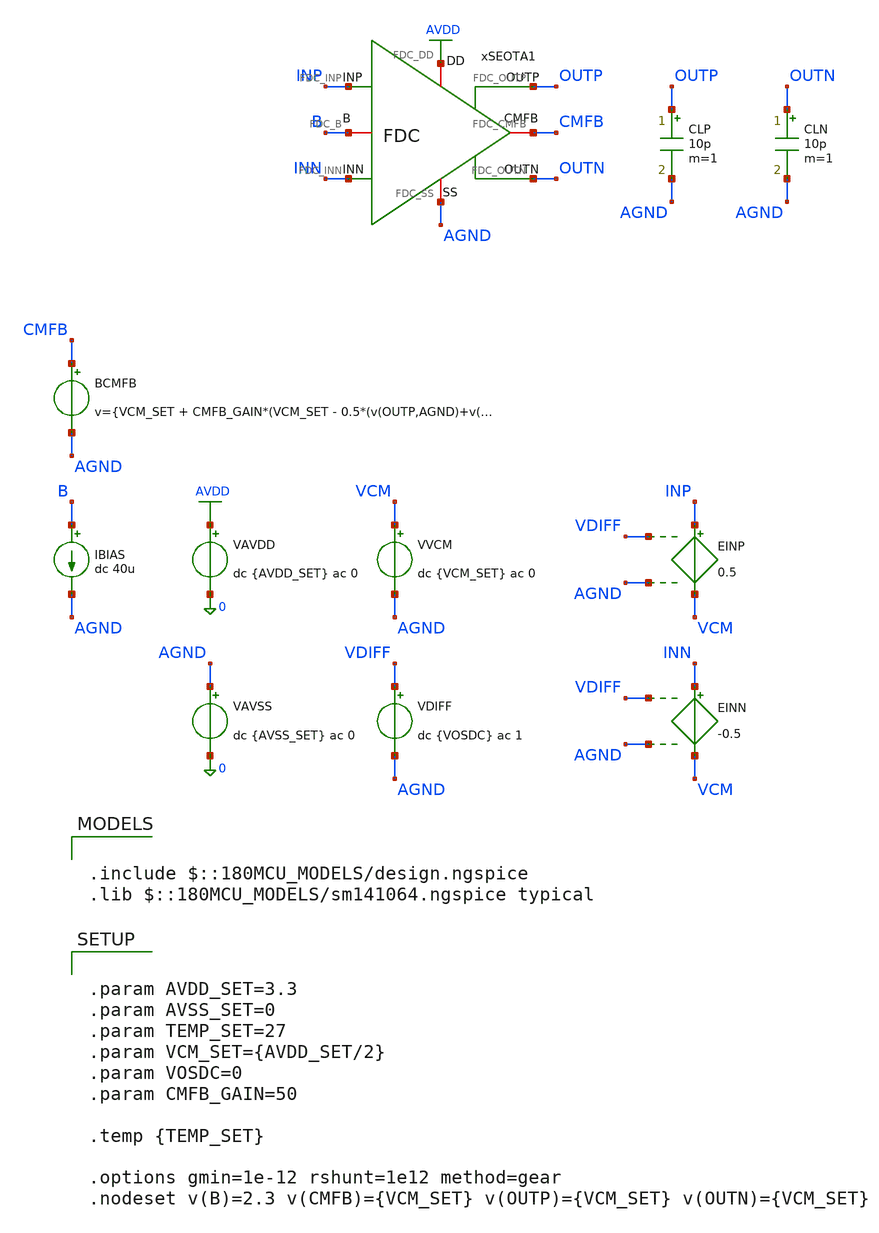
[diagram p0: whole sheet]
** sch_path: Design_Files/IC Design/Testbench/FD_OTA/FDC/Open_Loop/FDC_TB_OL_NOM.sch
**.subckt FDC_TB_OL_NOM
IBIAS B AGND dc 40u
VAVDD AVDD 0 dc {AVDD_SET} ac 0
.save i(vavdd)
CLP OUTP AGND 10p m=1
VVCM VCM AGND dc {VCM_SET} ac 0
VDIFF VDIFF AGND dc {VOSDC} ac 1
VAVSS AGND 0 dc {AVSS_SET} ac 0
.save i(vavss)
EINN INN VCM VDIFF AGND -0.5
EINP INP VCM VDIFF AGND 0.5
xSEOTA1 AVDD AGND INP INN OUTN B OUTP CMFB FDC
CLN OUTN AGND 10p m=1
BCMFB CMFB AGND v={VCM_SET + CMFB_GAIN*(VCM_SET - 0.5*(v(OUTP,AGND)+v(OUTN,AGND)))}
**** begin user architecture code

.include $::180MCU_MODELS/design.ngspice
.lib $::180MCU_MODELS/sm141064.ngspice typical



.control
destroy all
save all
set wr_vecnames
set wr_singlescale

shell mkdir -p
+ /foss/designs/ECG_Acquisition_IC/Measurement_Results/IC_Simulation/FD_OTA/FDC/NOM.Result_txt

shell rm -f
+ /foss/designs/ECG_Acquisition_IC/Measurement_Results/IC_Simulation/FD_OTA/FDC/NOM.Result_txt/NOM.ol_op.txt
shell rm -f
+ /foss/designs/ECG_Acquisition_IC/Measurement_Results/IC_Simulation/FD_OTA/FDC/NOM.Result_txt/NOM.ol_diff_tf.txt
shell rm -f
+ /foss/designs/ECG_Acquisition_IC/Measurement_Results/IC_Simulation/FD_OTA/FDC/NOM.Result_txt/NOM.ol_diff_ac.txt
shell rm -f
+ /foss/designs/ECG_Acquisition_IC/Measurement_Results/IC_Simulation/FD_OTA/FDC/NOM.Result_txt/NOM.ol_offset.txt
shell rm -f
+ /foss/designs/ECG_Acquisition_IC/Measurement_Results/IC_Simulation/FD_OTA/FDC/NOM.Result_txt/NOM.ol_icmr.txt
shell rm -f
+ /foss/designs/ECG_Acquisition_IC/Measurement_Results/IC_Simulation/FD_OTA/FDC/NOM.Result_txt/NOM.ol_cm_diff_ac.txt
shell rm -f
+ /foss/designs/ECG_Acquisition_IC/Measurement_Results/IC_Simulation/FD_OTA/FDC/NOM.Result_txt/NOM.ol_psrrp_diff_ac.txt
shell rm -f
+ /foss/designs/ECG_Acquisition_IC/Measurement_Results/IC_Simulation/FD_OTA/FDC/NOM.Result_txt/NOM.ol_psrrn_diff_ac.txt

let avdd_run = 3.3
let vcm_run  = avdd_run/2
let vos_run  = 0

* OP
alter @VVCM[DC] = $&vcm_run
alter @VDIFF[DC] = $&vos_run
alter @VVCM[ACMAG] = 0
alter @VDIFF[ACMAG] = 0
alter @VAVDD[ACMAG] = 0
alter @VAVSS[ACMAG] = 0

op

let op_vdd   = v(avdd) - v(agnd)
let op_vinp  = v(inp) - v(agnd)
let op_vinn  = v(inn) - v(agnd)
let op_voutp = v(outp) - v(agnd)
let op_voutn = v(outn) - v(agnd)
let op_ibias = 40e-6
let op_idd   = -vavdd#branch
let op_cmfb  = v(cmfb) - v(agnd)

wrdata
+ /foss/designs/ECG_Acquisition_IC/Measurement_Results/IC_Simulation/FD_OTA/FDC/NOM.Result_txt/NOM.ol_op.txt op_vdd op_vinp op_vinn op_voutp op_voutn op_ibias op_idd op_cmfb

* DC TF by low-frequency AC point
alter @VVCM[ACMAG] = 0
alter @VDIFF[ACMAG] = 1
alter @VDIFF[ACPHASE] = 0
alter @VAVDD[ACMAG] = 0
alter @VAVSS[ACMAG] = 0

ac lin 1 1 1

let tf_vod = v(outp) - v(outn)
let ad_dc = mag(tf_vod)

wrdata
+ /foss/designs/ECG_Acquisition_IC/Measurement_Results/IC_Simulation/FD_OTA/FDC/NOM.Result_txt/NOM.ol_diff_tf.txt ad_dc

* Differential AC
ac dec 200 1 1G

let ad_vod  = v(outp) - v(outn)
let ad_real = real(ad_vod)
let ad_imag = imag(ad_vod)

wrdata
+ /foss/designs/ECG_Acquisition_IC/Measurement_Results/IC_Simulation/FD_OTA/FDC/NOM.Result_txt/NOM.ol_diff_ac.txt ad_real ad_imag

* Offset sweep
alter @VVCM[DC] = $&vcm_run
alter @VDIFF[ACMAG] = 0

dc VDIFF -0.02 0.02 0.00001

let off_vinp  = v(inp) - v(agnd)
let off_vinn  = v(inn) - v(agnd)
let off_voutp = v(outp) - v(agnd)
let off_voutn = v(outn) - v(agnd)
let off_idd   = -vavdd#branch
let off_cmfb  = v(cmfb) - v(agnd)

wrdata
+ /foss/designs/ECG_Acquisition_IC/Measurement_Results/IC_Simulation/FD_OTA/FDC/NOM.Result_txt/NOM.ol_offset.txt off_vinp off_vinn off_voutp off_voutn off_idd off_cmfb

* ICMR sweep
alter @VVCM[ACMAG] = 0
alter @VDIFF[ACMAG] = 0
alter @VAVDD[ACMAG] = 0
alter @VAVSS[ACMAG] = 0

dc VVCM 0 $&avdd_run 0.01 VDIFF -0.2 0.2 0.001

let icmr_vcm   = v(vcm) - v(agnd)
let icmr_vdiff = v(vdiff) - v(agnd)
let icmr_vinp  = v(inp) - v(agnd)
let icmr_vinn  = v(inn) - v(agnd)
let icmr_voutp = v(outp) - v(agnd)
let icmr_voutn = v(outn) - v(agnd)
let icmr_idd   = -vavdd#branch
let icmr_cmfb  = v(cmfb) - v(agnd)

wrdata
+ /foss/designs/ECG_Acquisition_IC/Measurement_Results/IC_Simulation/FD_OTA/FDC/NOM.Result_txt/NOM.ol_icmr.txt icmr_vcm icmr_vdiff icmr_vinp icmr_vinn icmr_voutp icmr_voutn icmr_idd icmr_cmfb

* CM to differential AC
alter @VVCM[DC] = $&vcm_run
alter @VDIFF[DC] = $&vos_run
alter @VVCM[ACMAG] = 1
alter @VVCM[ACPHASE] = 0
alter @VDIFF[ACMAG] = 0
alter @VAVDD[ACMAG] = 0
alter @VAVSS[ACMAG] = 0

ac dec 200 1 1G

let acm_vod  = v(outp) - v(outn)
let acm_real = real(acm_vod)
let acm_imag = imag(acm_vod)

wrdata
+ /foss/designs/ECG_Acquisition_IC/Measurement_Results/IC_Simulation/FD_OTA/FDC/NOM.Result_txt/NOM.ol_cm_diff_ac.txt acm_real acm_imag

* PSRR+ differential
alter @VVCM[ACMAG] = 0
alter @VDIFF[ACMAG] = 0
alter @VAVDD[ACMAG] = 1
alter @VAVDD[ACPHASE] = 0
alter @VAVSS[ACMAG] = 0

ac dec 200 1 1G

let psrrp_vod  = v(outp) - v(outn)
let psrrp_real = real(psrrp_vod)
let psrrp_imag = imag(psrrp_vod)

wrdata
+ /foss/designs/ECG_Acquisition_IC/Measurement_Results/IC_Simulation/FD_OTA/FDC/NOM.Result_txt/NOM.ol_psrrp_diff_ac.txt psrrp_real psrrp_imag

* PSRR- differential
alter @VVCM[ACMAG] = 0
alter @VDIFF[ACMAG] = 0
alter @VAVDD[ACMAG] = 0
alter @VAVSS[ACMAG] = 1
alter @VAVSS[ACPHASE] = 0

ac dec 200 1 1G

let psrrn_vod  = v(outp) - v(outn)
let psrrn_real = real(psrrn_vod)
let psrrn_imag = imag(psrrn_vod)

wrdata
+ /foss/designs/ECG_Acquisition_IC/Measurement_Results/IC_Simulation/FD_OTA/FDC/NOM.Result_txt/NOM.ol_psrrn_diff_ac.txt psrrn_real psrrn_imag

.endc




.param AVDD_SET=3.3
.param AVSS_SET=0
.param TEMP_SET=27
.param VCM_SET={AVDD_SET/2}
.param VOSDC=0
.param CMFB_GAIN=50

.temp {TEMP_SET}

.options gmin=1e-12 rshunt=1e12 method=gear
.nodeset v(B)=2.3 v(CMFB)={VCM_SET} v(OUTP)={VCM_SET} v(OUTN)={VCM_SET}


**** end user architecture code
**.ends

* expanding   symbol:  ECG_Acquisition_IC/Design_Files/IC Design/Schematic/FD_OTA/FDC/FDC.sym # of
*+ pins=8
** sym_path: Design_Files/IC Design/Schematic/FD_OTA/FDC/FDC.sym
** sch_path: Design_Files/IC Design/Schematic/FD_OTA/FDC/FDC.sch
.subckt FDC FDC_DD FDC_SS FDC_INP FDC_INN FDC_OUTN FDC_B FDC_OUTP FDC_CMFB
*.iopin FDC_DD
*.iopin FDC_SS
*.ipin FDC_INP
*.ipin FDC_INN
*.opin FDC_OUTP
*.iopin FDC_B
*.opin FDC_OUTN
*.iopin FDC_CMFB
XM4 net1 FDC_CMFB FDC_SS FDC_SS nfet_03v3 L=2u W=2u nf=1 ad='int((nf+1)/2) * W/nf * 0.18u' as='int((nf+2)/2) * W/nf * 0.18u'
+ pd='2*int((nf+1)/2) * (W/nf + 0.18u)' ps='2*int((nf+2)/2) * (W/nf + 0.18u)' nrd='0.18u / W' nrs='0.18u / W'
+ sa=0 sb=0 sd=0 m=2
XM3 net4 FDC_CMFB FDC_SS FDC_SS nfet_03v3 L=2u W=2u nf=1 ad='int((nf+1)/2) * W/nf * 0.18u' as='int((nf+2)/2) * W/nf * 0.18u'
+ pd='2*int((nf+1)/2) * (W/nf + 0.18u)' ps='2*int((nf+2)/2) * (W/nf + 0.18u)' nrd='0.18u / W' nrs='0.18u / W'
+ sa=0 sb=0 sd=0 m=2
XM1 net3 FDC_INN net4 FDC_SS pfet_03v3 L=1u W=32u nf=16 ad='int((nf+1)/2) * W/nf * 0.18u' as='int((nf+2)/2) * W/nf * 0.18u'
+ pd='2*int((nf+1)/2) * (W/nf + 0.18u)' ps='2*int((nf+2)/2) * (W/nf + 0.18u)' nrd='0.18u / W' nrs='0.18u / W'
+ sa=0 sb=0 sd=0 m=2
XM2 net3 FDC_INP net1 FDC_SS pfet_03v3 L=1u W=32u nf=16 ad='int((nf+1)/2) * W/nf * 0.18u' as='int((nf+2)/2) * W/nf * 0.18u'
+ pd='2*int((nf+1)/2) * (W/nf + 0.18u)' ps='2*int((nf+2)/2) * (W/nf + 0.18u)' nrd='0.18u / W' nrs='0.18u / W'
+ sa=0 sb=0 sd=0 m=2
XM6 FDC_OUTP FDC_B FDC_SS FDC_SS pfet_03v3 L=0.5u W=56u nf=28 ad='int((nf+1)/2) * W/nf * 0.18u' as='int((nf+2)/2) * W/nf * 0.18u'
+ pd='2*int((nf+1)/2) * (W/nf + 0.18u)' ps='2*int((nf+2)/2) * (W/nf + 0.18u)' nrd='0.18u / W' nrs='0.18u / W'
+ sa=0 sb=0 sd=0 m=2
Rz net1 net2 0.5k m=1
XM5 net3 FDC_B FDC_SS FDC_SS pfet_03v3 L=2u W=20u nf=10 ad='int((nf+1)/2) * W/nf * 0.18u' as='int((nf+2)/2) * W/nf * 0.18u'
+ pd='2*int((nf+1)/2) * (W/nf + 0.18u)' ps='2*int((nf+2)/2) * (W/nf + 0.18u)' nrd='0.18u / W' nrs='0.18u / W'
+ sa=0 sb=0 sd=0 m=2
XM7 FDC_OUTP net1 FDC_SS FDC_SS nfet_03v3 L=0.5u W=16u nf=8 ad='int((nf+1)/2) * W/nf * 0.18u' as='int((nf+2)/2) * W/nf * 0.18u'
+ pd='2*int((nf+1)/2) * (W/nf + 0.18u)' ps='2*int((nf+2)/2) * (W/nf + 0.18u)' nrd='0.18u / W' nrs='0.18u / W'
+ sa=0 sb=0 sd=0 m=2
XM10 FDC_B FDC_B FDC_SS FDC_SS pfet_03v3 L=2u W=50u nf=25 ad='int((nf+1)/2) * W/nf * 0.18u' as='int((nf+2)/2) * W/nf * 0.18u'
+ pd='2*int((nf+1)/2) * (W/nf + 0.18u)' ps='2*int((nf+2)/2) * (W/nf + 0.18u)' nrd='0.18u / W' nrs='0.18u / W'
+ sa=0 sb=0 sd=0 m=2
Cc net2 FDC_OUTP 2p m=1
XM8 FDC_OUTN FDC_B FDC_SS FDC_SS pfet_03v3 L=0.5u W=56u nf=28 ad='int((nf+1)/2) * W/nf * 0.18u' as='int((nf+2)/2) * W/nf * 0.18u'
+ pd='2*int((nf+1)/2) * (W/nf + 0.18u)' ps='2*int((nf+2)/2) * (W/nf + 0.18u)' nrd='0.18u / W' nrs='0.18u / W'
+ sa=0 sb=0 sd=0 m=2
Rz1 net4 net5 0.5k m=1
XM9 FDC_OUTN net4 FDC_SS FDC_SS nfet_03v3 L=0.5u W=16u nf=8 ad='int((nf+1)/2) * W/nf * 0.18u' as='int((nf+2)/2) * W/nf * 0.18u'
+ pd='2*int((nf+1)/2) * (W/nf + 0.18u)' ps='2*int((nf+2)/2) * (W/nf + 0.18u)' nrd='0.18u / W' nrs='0.18u / W'
+ sa=0 sb=0 sd=0 m=2
Cc1 net5 FDC_OUTN 2p m=1
.ends

.GLOBAL AVDD
.end
